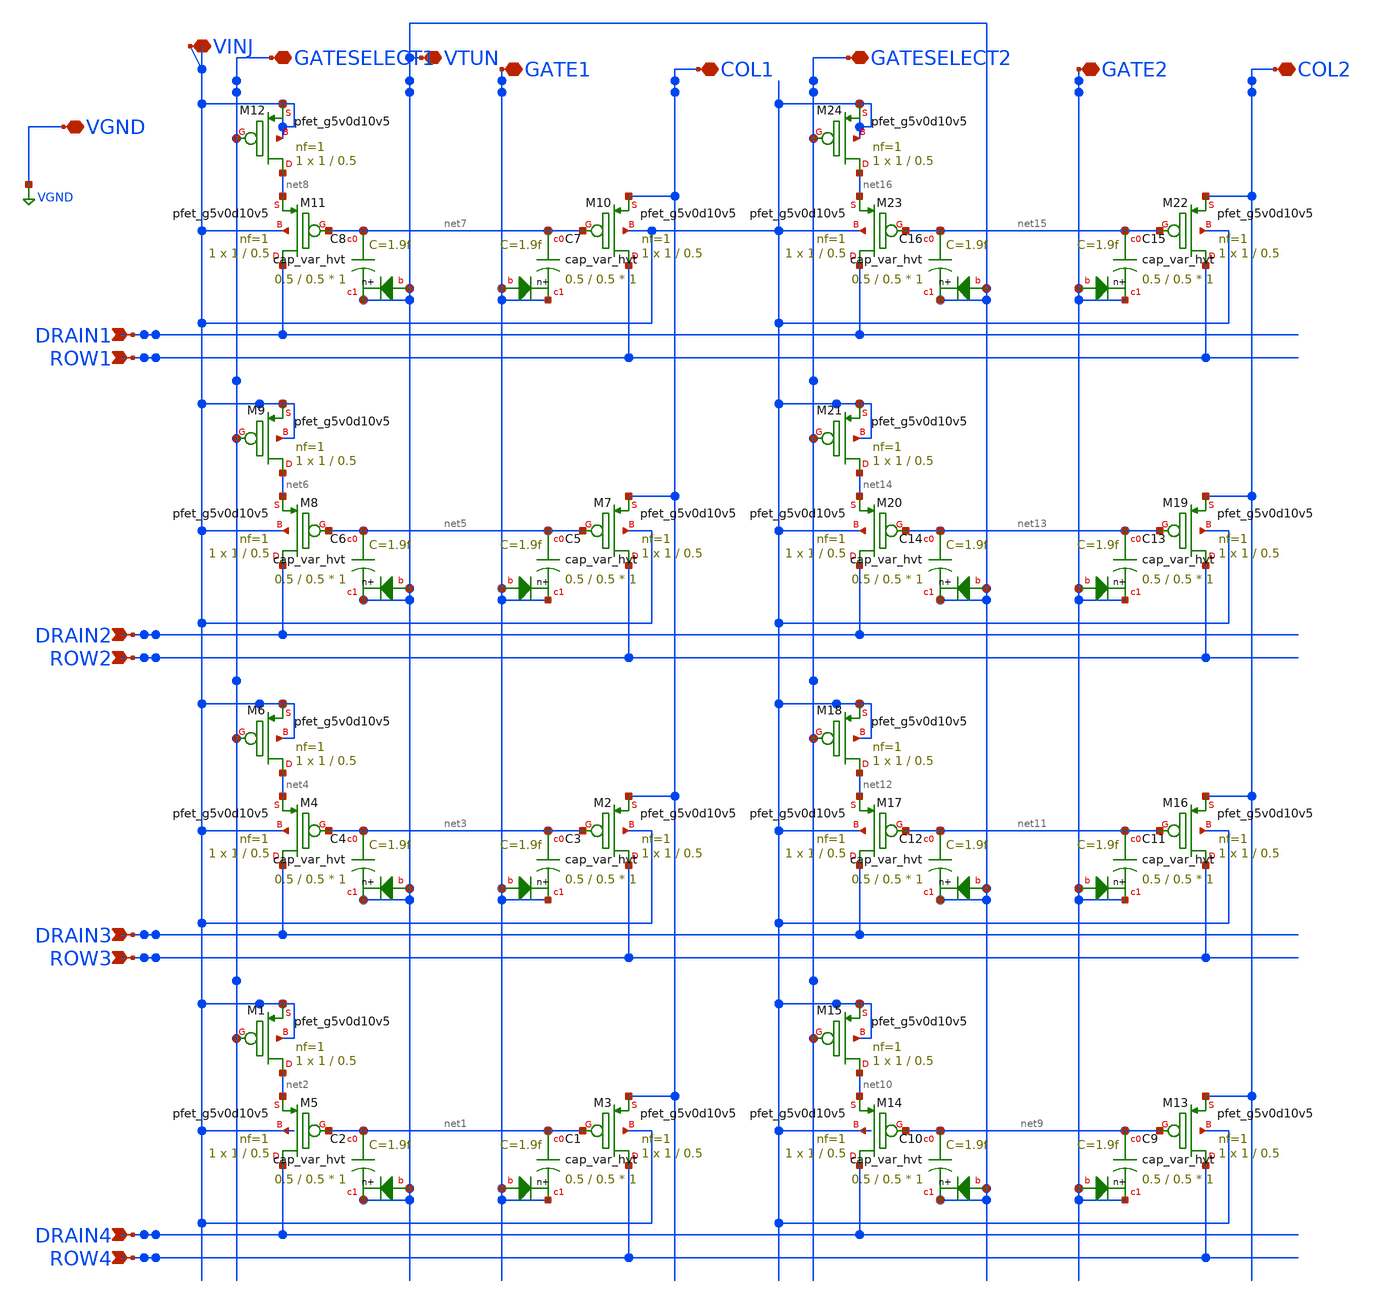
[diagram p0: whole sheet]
** sch_path: libs.ref/sky130_hilas_sc/xschem/sky130_hilas_swc4x2cell.sch
**.subckt sky130_hilas_swc4x2cell DRAIN1 ROW1 DRAIN2 ROW2 DRAIN3 ROW3 DRAIN4 ROW4 COL1 GATE1 VTUN
*+ GATESELECT1 VINJ COL2 GATE2 GATESELECT2 VGND
*.ipin DRAIN1
*.ipin ROW1
*.ipin DRAIN2
*.ipin ROW2
*.ipin DRAIN3
*.ipin ROW3
*.ipin DRAIN4
*.ipin ROW4
*.iopin COL1
*.iopin GATE1
*.iopin VTUN
*.iopin GATESELECT1
*.iopin VINJ
*.iopin COL2
*.iopin GATE2
*.iopin GATESELECT2
*.iopin VGND
XM3 ROW4 net1 COL1 VINJ sky130_fd_pr__pfet_g5v0d10v5 L=0.5 W=1 nf=1 ad='int((nf+1)/2) * W/nf * 0.29'
+ as='int((nf+2)/2) * W/nf * 0.29' pd='2*int((nf+1)/2) * (W/nf + 0.29)' ps='2*int((nf+2)/2) * (W/nf + 0.29)'
+ nrd='0.29 / W' nrs='0.29 / W' sa=0 sb=0 sd=0 mult=1 m=1
XC1 net1 GATE1 GATE1 sky130_fd_pr__cap_var_hvt W=0.5 L=0.5 VM=1 m=1
XM5 DRAIN4 net1 net2 VINJ sky130_fd_pr__pfet_g5v0d10v5 L=0.5 W=1 nf=1 ad='int((nf+1)/2) * W/nf * 0.29'
+ as='int((nf+2)/2) * W/nf * 0.29' pd='2*int((nf+1)/2) * (W/nf + 0.29)' ps='2*int((nf+2)/2) * (W/nf + 0.29)'
+ nrd='0.29 / W' nrs='0.29 / W' sa=0 sb=0 sd=0 mult=1 m=1
XC2 net1 VTUN VTUN sky130_fd_pr__cap_var_hvt W=0.5 L=0.5 VM=1 m=1
XM1 net2 GATESELECT1 VINJ VINJ sky130_fd_pr__pfet_g5v0d10v5 L=0.5 W=1 nf=1 ad='int((nf+1)/2) * W/nf * 0.29'
+ as='int((nf+2)/2) * W/nf * 0.29' pd='2*int((nf+1)/2) * (W/nf + 0.29)' ps='2*int((nf+2)/2) * (W/nf + 0.29)'
+ nrd='0.29 / W' nrs='0.29 / W' sa=0 sb=0 sd=0 mult=1 m=1
XM2 ROW3 net3 COL1 VINJ sky130_fd_pr__pfet_g5v0d10v5 L=0.5 W=1 nf=1 ad='int((nf+1)/2) * W/nf * 0.29'
+ as='int((nf+2)/2) * W/nf * 0.29' pd='2*int((nf+1)/2) * (W/nf + 0.29)' ps='2*int((nf+2)/2) * (W/nf + 0.29)'
+ nrd='0.29 / W' nrs='0.29 / W' sa=0 sb=0 sd=0 mult=1 m=1
XC3 net3 GATE1 GATE1 sky130_fd_pr__cap_var_hvt W=0.5 L=0.5 VM=1 m=1
XM4 DRAIN3 net3 net4 VINJ sky130_fd_pr__pfet_g5v0d10v5 L=0.5 W=1 nf=1 ad='int((nf+1)/2) * W/nf * 0.29'
+ as='int((nf+2)/2) * W/nf * 0.29' pd='2*int((nf+1)/2) * (W/nf + 0.29)' ps='2*int((nf+2)/2) * (W/nf + 0.29)'
+ nrd='0.29 / W' nrs='0.29 / W' sa=0 sb=0 sd=0 mult=1 m=1
XC4 net3 VTUN VTUN sky130_fd_pr__cap_var_hvt W=0.5 L=0.5 VM=1 m=1
XM6 net4 GATESELECT1 VINJ VINJ sky130_fd_pr__pfet_g5v0d10v5 L=0.5 W=1 nf=1 ad='int((nf+1)/2) * W/nf * 0.29'
+ as='int((nf+2)/2) * W/nf * 0.29' pd='2*int((nf+1)/2) * (W/nf + 0.29)' ps='2*int((nf+2)/2) * (W/nf + 0.29)'
+ nrd='0.29 / W' nrs='0.29 / W' sa=0 sb=0 sd=0 mult=1 m=1
XM7 ROW2 net5 COL1 VINJ sky130_fd_pr__pfet_g5v0d10v5 L=0.5 W=1 nf=1 ad='int((nf+1)/2) * W/nf * 0.29'
+ as='int((nf+2)/2) * W/nf * 0.29' pd='2*int((nf+1)/2) * (W/nf + 0.29)' ps='2*int((nf+2)/2) * (W/nf + 0.29)'
+ nrd='0.29 / W' nrs='0.29 / W' sa=0 sb=0 sd=0 mult=1 m=1
XC5 net5 GATE1 GATE1 sky130_fd_pr__cap_var_hvt W=0.5 L=0.5 VM=1 m=1
XM8 DRAIN2 net5 net6 VINJ sky130_fd_pr__pfet_g5v0d10v5 L=0.5 W=1 nf=1 ad='int((nf+1)/2) * W/nf * 0.29'
+ as='int((nf+2)/2) * W/nf * 0.29' pd='2*int((nf+1)/2) * (W/nf + 0.29)' ps='2*int((nf+2)/2) * (W/nf + 0.29)'
+ nrd='0.29 / W' nrs='0.29 / W' sa=0 sb=0 sd=0 mult=1 m=1
XC6 net5 VTUN VTUN sky130_fd_pr__cap_var_hvt W=0.5 L=0.5 VM=1 m=1
XM9 net6 GATESELECT1 VINJ VINJ sky130_fd_pr__pfet_g5v0d10v5 L=0.5 W=1 nf=1 ad='int((nf+1)/2) * W/nf * 0.29'
+ as='int((nf+2)/2) * W/nf * 0.29' pd='2*int((nf+1)/2) * (W/nf + 0.29)' ps='2*int((nf+2)/2) * (W/nf + 0.29)'
+ nrd='0.29 / W' nrs='0.29 / W' sa=0 sb=0 sd=0 mult=1 m=1
XM10 ROW1 net7 COL1 VINJ sky130_fd_pr__pfet_g5v0d10v5 L=0.5 W=1 nf=1 ad='int((nf+1)/2) * W/nf * 0.29'
+ as='int((nf+2)/2) * W/nf * 0.29' pd='2*int((nf+1)/2) * (W/nf + 0.29)' ps='2*int((nf+2)/2) * (W/nf + 0.29)'
+ nrd='0.29 / W' nrs='0.29 / W' sa=0 sb=0 sd=0 mult=1 m=1
XC7 net7 GATE1 GATE1 sky130_fd_pr__cap_var_hvt W=0.5 L=0.5 VM=1 m=1
XM11 DRAIN1 net7 net8 VINJ sky130_fd_pr__pfet_g5v0d10v5 L=0.5 W=1 nf=1 ad='int((nf+1)/2) * W/nf * 0.29'
+ as='int((nf+2)/2) * W/nf * 0.29' pd='2*int((nf+1)/2) * (W/nf + 0.29)' ps='2*int((nf+2)/2) * (W/nf + 0.29)'
+ nrd='0.29 / W' nrs='0.29 / W' sa=0 sb=0 sd=0 mult=1 m=1
XC8 net7 VTUN VTUN sky130_fd_pr__cap_var_hvt W=0.5 L=0.5 VM=1 m=1
XM12 net8 GATESELECT1 VINJ VINJ sky130_fd_pr__pfet_g5v0d10v5 L=0.5 W=1 nf=1 ad='int((nf+1)/2) * W/nf * 0.29'
+ as='int((nf+2)/2) * W/nf * 0.29' pd='2*int((nf+1)/2) * (W/nf + 0.29)' ps='2*int((nf+2)/2) * (W/nf + 0.29)'
+ nrd='0.29 / W' nrs='0.29 / W' sa=0 sb=0 sd=0 mult=1 m=1
XM13 ROW4 net9 COL2 VINJ sky130_fd_pr__pfet_g5v0d10v5 L=0.5 W=1 nf=1 ad='int((nf+1)/2) * W/nf * 0.29'
+ as='int((nf+2)/2) * W/nf * 0.29' pd='2*int((nf+1)/2) * (W/nf + 0.29)' ps='2*int((nf+2)/2) * (W/nf + 0.29)'
+ nrd='0.29 / W' nrs='0.29 / W' sa=0 sb=0 sd=0 mult=1 m=1
XC9 net9 GATE2 GATE2 sky130_fd_pr__cap_var_hvt W=0.5 L=0.5 VM=1 m=1
XM14 DRAIN4 net9 net10 VINJ sky130_fd_pr__pfet_g5v0d10v5 L=0.5 W=1 nf=1 ad='int((nf+1)/2) * W/nf * 0.29'
+ as='int((nf+2)/2) * W/nf * 0.29' pd='2*int((nf+1)/2) * (W/nf + 0.29)' ps='2*int((nf+2)/2) * (W/nf + 0.29)'
+ nrd='0.29 / W' nrs='0.29 / W' sa=0 sb=0 sd=0 mult=1 m=1
XC10 net9 VTUN VTUN sky130_fd_pr__cap_var_hvt W=0.5 L=0.5 VM=1 m=1
XM15 net10 GATESELECT2 VINJ VINJ sky130_fd_pr__pfet_g5v0d10v5 L=0.5 W=1 nf=1 ad='int((nf+1)/2) * W/nf * 0.29'
+ as='int((nf+2)/2) * W/nf * 0.29' pd='2*int((nf+1)/2) * (W/nf + 0.29)' ps='2*int((nf+2)/2) * (W/nf + 0.29)'
+ nrd='0.29 / W' nrs='0.29 / W' sa=0 sb=0 sd=0 mult=1 m=1
XM16 ROW3 net11 COL2 VINJ sky130_fd_pr__pfet_g5v0d10v5 L=0.5 W=1 nf=1 ad='int((nf+1)/2) * W/nf * 0.29'
+ as='int((nf+2)/2) * W/nf * 0.29' pd='2*int((nf+1)/2) * (W/nf + 0.29)' ps='2*int((nf+2)/2) * (W/nf + 0.29)'
+ nrd='0.29 / W' nrs='0.29 / W' sa=0 sb=0 sd=0 mult=1 m=1
XC11 net11 GATE2 GATE2 sky130_fd_pr__cap_var_hvt W=0.5 L=0.5 VM=1 m=1
XM17 DRAIN3 net11 net12 VINJ sky130_fd_pr__pfet_g5v0d10v5 L=0.5 W=1 nf=1 ad='int((nf+1)/2) * W/nf * 0.29'
+ as='int((nf+2)/2) * W/nf * 0.29' pd='2*int((nf+1)/2) * (W/nf + 0.29)' ps='2*int((nf+2)/2) * (W/nf + 0.29)'
+ nrd='0.29 / W' nrs='0.29 / W' sa=0 sb=0 sd=0 mult=1 m=1
XC12 net11 VTUN VTUN sky130_fd_pr__cap_var_hvt W=0.5 L=0.5 VM=1 m=1
XM18 net12 GATESELECT2 VINJ VINJ sky130_fd_pr__pfet_g5v0d10v5 L=0.5 W=1 nf=1 ad='int((nf+1)/2) * W/nf * 0.29'
+ as='int((nf+2)/2) * W/nf * 0.29' pd='2*int((nf+1)/2) * (W/nf + 0.29)' ps='2*int((nf+2)/2) * (W/nf + 0.29)'
+ nrd='0.29 / W' nrs='0.29 / W' sa=0 sb=0 sd=0 mult=1 m=1
XM19 ROW2 net13 COL2 VINJ sky130_fd_pr__pfet_g5v0d10v5 L=0.5 W=1 nf=1 ad='int((nf+1)/2) * W/nf * 0.29'
+ as='int((nf+2)/2) * W/nf * 0.29' pd='2*int((nf+1)/2) * (W/nf + 0.29)' ps='2*int((nf+2)/2) * (W/nf + 0.29)'
+ nrd='0.29 / W' nrs='0.29 / W' sa=0 sb=0 sd=0 mult=1 m=1
XC13 net13 GATE2 GATE2 sky130_fd_pr__cap_var_hvt W=0.5 L=0.5 VM=1 m=1
XM20 DRAIN2 net13 net14 VINJ sky130_fd_pr__pfet_g5v0d10v5 L=0.5 W=1 nf=1 ad='int((nf+1)/2) * W/nf * 0.29'
+ as='int((nf+2)/2) * W/nf * 0.29' pd='2*int((nf+1)/2) * (W/nf + 0.29)' ps='2*int((nf+2)/2) * (W/nf + 0.29)'
+ nrd='0.29 / W' nrs='0.29 / W' sa=0 sb=0 sd=0 mult=1 m=1
XC14 net13 VTUN VTUN sky130_fd_pr__cap_var_hvt W=0.5 L=0.5 VM=1 m=1
XM21 net14 GATESELECT2 VINJ VINJ sky130_fd_pr__pfet_g5v0d10v5 L=0.5 W=1 nf=1 ad='int((nf+1)/2) * W/nf * 0.29'
+ as='int((nf+2)/2) * W/nf * 0.29' pd='2*int((nf+1)/2) * (W/nf + 0.29)' ps='2*int((nf+2)/2) * (W/nf + 0.29)'
+ nrd='0.29 / W' nrs='0.29 / W' sa=0 sb=0 sd=0 mult=1 m=1
XM22 ROW1 net15 COL2 VINJ sky130_fd_pr__pfet_g5v0d10v5 L=0.5 W=1 nf=1 ad='int((nf+1)/2) * W/nf * 0.29'
+ as='int((nf+2)/2) * W/nf * 0.29' pd='2*int((nf+1)/2) * (W/nf + 0.29)' ps='2*int((nf+2)/2) * (W/nf + 0.29)'
+ nrd='0.29 / W' nrs='0.29 / W' sa=0 sb=0 sd=0 mult=1 m=1
XC15 net15 GATE2 GATE2 sky130_fd_pr__cap_var_hvt W=0.5 L=0.5 VM=1 m=1
XM23 DRAIN1 net15 net16 VINJ sky130_fd_pr__pfet_g5v0d10v5 L=0.5 W=1 nf=1 ad='int((nf+1)/2) * W/nf * 0.29'
+ as='int((nf+2)/2) * W/nf * 0.29' pd='2*int((nf+1)/2) * (W/nf + 0.29)' ps='2*int((nf+2)/2) * (W/nf + 0.29)'
+ nrd='0.29 / W' nrs='0.29 / W' sa=0 sb=0 sd=0 mult=1 m=1
XC16 net15 VTUN VTUN sky130_fd_pr__cap_var_hvt W=0.5 L=0.5 VM=1 m=1
XM24 net16 GATESELECT2 VINJ VINJ sky130_fd_pr__pfet_g5v0d10v5 L=0.5 W=1 nf=1 ad='int((nf+1)/2) * W/nf * 0.29'
+ as='int((nf+2)/2) * W/nf * 0.29' pd='2*int((nf+1)/2) * (W/nf + 0.29)' ps='2*int((nf+2)/2) * (W/nf + 0.29)'
+ nrd='0.29 / W' nrs='0.29 / W' sa=0 sb=0 sd=0 mult=1 m=1
**.ends
.GLOBAL VGND
.end
